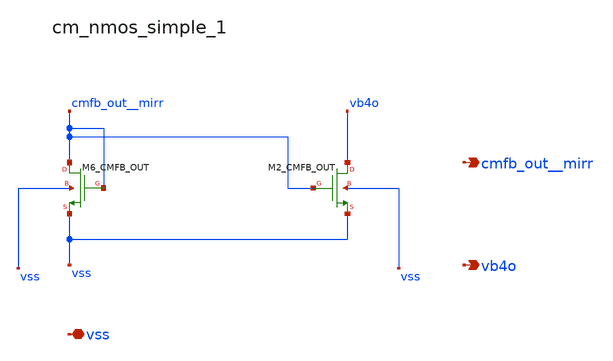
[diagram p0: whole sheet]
** sch_path: analog-db/raw/amp_035_fan_chopper_cmfb_dual/hier/blocks/cm_nmos_simple_1.sch
**.subckt cm_nmos_simple_1 vss cmfb_out__mirr vb4o
*.iopin vss
*.opin cmfb_out__mirr
*.opin vb4o
XM2_CMFB_OUT vb4o cmfb_out__mirr vss vss sg13_lv_nmos w=x_dut_xm2_cmfb_out_w l=x_dut_xm2_cmfb_out_l
+ ng=1 m=x_dut_xm2_cmfb_out_m
XM6_CMFB_OUT cmfb_out__mirr cmfb_out__mirr vss vss sg13_lv_nmos w=x_dut_xm6_cmfb_out_w
+ l=x_dut_xm6_cmfb_out_l ng=1 m=x_dut_xm6_cmfb_out_m
**.ends
.end
